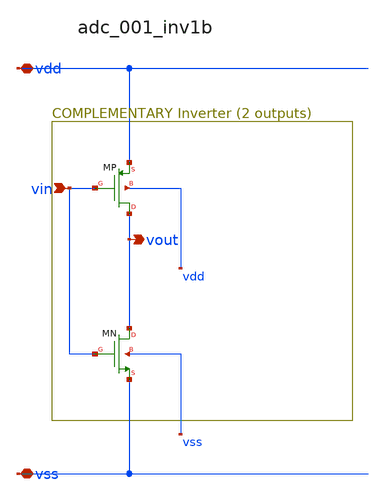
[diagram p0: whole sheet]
** sch_path: analog-db/raw/adc_001_inv1b/adc_001_inv1b_annotated.sch
**.subckt adc_001_inv1b_annotated vin vdd vss vout
*.ipin vin
*.iopin vdd
*.iopin vss
*.opin vout
XMN vout vin vss vss sg13_lv_nmos w=x_dut_xmn_w l=x_dut_xmn_l ng=1 m=x_dut_xmn_m
XMP vout vin vdd vdd sg13_lv_pmos w=x_dut_xmp_w l=x_dut_xmp_l ng=1 m=x_dut_xmp_m
**.ends
.end
